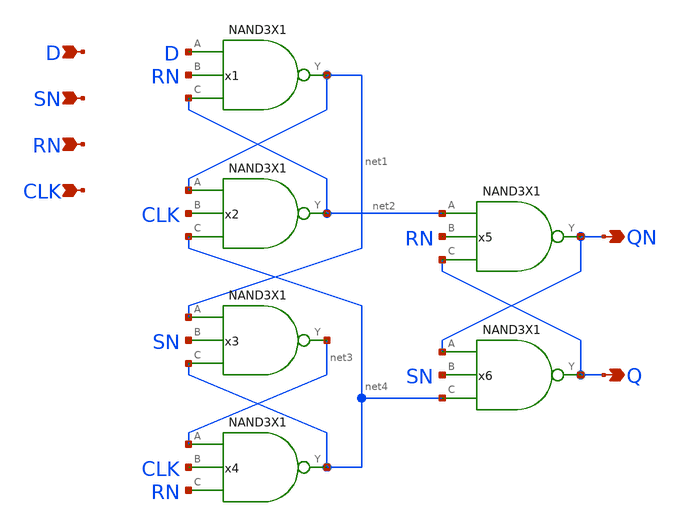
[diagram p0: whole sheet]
** sch_path: lib/xschem/DFFSNRNX1.sch
**.subckt DFFSNRNX1 D QN SN CLK Q RN
*.ipin D
*.opin QN
*.ipin SN
*.ipin CLK
*.opin Q
*.ipin RN
x3 net3 net1 SN net4 NAND3X1
x2 net2 net1 CLK net4 NAND3X1
x6 Q QN SN net4 NAND3X1
x1 net1 D RN net2 NAND3X1
x4 net4 net3 CLK RN NAND3X1
x5 QN net2 RN Q NAND3X1
**.ends

* expanding   symbol:  NAND3X1.sym # of pins=4
** sym_path: lib/xschem/NAND3X1.sym
** sch_path: lib/xschem/NAND3X1.sch
.subckt NAND3X1 Y A B C
*.ipin A
*.opin Y
*.ipin B
*.ipin C
XM1 net2 C GND GND sky130_fd_pr__nfet_01v8 L=0.15 W=3 nf=1 ad='int((nf+1)/2) * W/nf * 0.29' as='int((nf+2)/2) * W/nf * 0.29'
+ pd='2*int((nf+1)/2) * (W/nf + 0.29)' ps='2*int((nf+2)/2) * (W/nf + 0.29)' nrd='0.29 / W' nrs='0.29 / W'
+ sa=0 sb=0 sd=0 mult=1 m=1
XM2 Y A VDD VDD sky130_fd_pr__pfet_01v8 L=0.15 W=2 nf=1 ad='int((nf+1)/2) * W/nf * 0.29' as='int((nf+2)/2) * W/nf * 0.29'
+ pd='2*int((nf+1)/2) * (W/nf + 0.29)' ps='2*int((nf+2)/2) * (W/nf + 0.29)' nrd='0.29 / W' nrs='0.29 / W'
+ sa=0 sb=0 sd=0 mult=1 m=1
XM3 net1 B net2 GND sky130_fd_pr__nfet_01v8 L=0.15 W=3 nf=1 ad='int((nf+1)/2) * W/nf * 0.29' as='int((nf+2)/2) * W/nf * 0.29'
+ pd='2*int((nf+1)/2) * (W/nf + 0.29)' ps='2*int((nf+2)/2) * (W/nf + 0.29)' nrd='0.29 / W' nrs='0.29 / W'
+ sa=0 sb=0 sd=0 mult=1 m=1
XM4 Y A net1 GND sky130_fd_pr__nfet_01v8 L=0.15 W=3 nf=1 ad='int((nf+1)/2) * W/nf * 0.29' as='int((nf+2)/2) * W/nf * 0.29'
+ pd='2*int((nf+1)/2) * (W/nf + 0.29)' ps='2*int((nf+2)/2) * (W/nf + 0.29)' nrd='0.29 / W' nrs='0.29 / W'
+ sa=0 sb=0 sd=0 mult=1 m=1
XM5 Y A VDD VDD sky130_fd_pr__pfet_01v8 L=0.15 W=2 nf=1 ad='int((nf+1)/2) * W/nf * 0.29' as='int((nf+2)/2) * W/nf * 0.29'
+ pd='2*int((nf+1)/2) * (W/nf + 0.29)' ps='2*int((nf+2)/2) * (W/nf + 0.29)' nrd='0.29 / W' nrs='0.29 / W'
+ sa=0 sb=0 sd=0 mult=1 m=1
XM6 Y B VDD VDD sky130_fd_pr__pfet_01v8 L=0.15 W=2 nf=1 ad='int((nf+1)/2) * W/nf * 0.29' as='int((nf+2)/2) * W/nf * 0.29'
+ pd='2*int((nf+1)/2) * (W/nf + 0.29)' ps='2*int((nf+2)/2) * (W/nf + 0.29)' nrd='0.29 / W' nrs='0.29 / W'
+ sa=0 sb=0 sd=0 mult=1 m=1
XM7 Y B VDD VDD sky130_fd_pr__pfet_01v8 L=0.15 W=2 nf=1 ad='int((nf+1)/2) * W/nf * 0.29' as='int((nf+2)/2) * W/nf * 0.29'
+ pd='2*int((nf+1)/2) * (W/nf + 0.29)' ps='2*int((nf+2)/2) * (W/nf + 0.29)' nrd='0.29 / W' nrs='0.29 / W'
+ sa=0 sb=0 sd=0 mult=1 m=1
XM8 Y C VDD VDD sky130_fd_pr__pfet_01v8 L=0.15 W=2 nf=1 ad='int((nf+1)/2) * W/nf * 0.29' as='int((nf+2)/2) * W/nf * 0.29'
+ pd='2*int((nf+1)/2) * (W/nf + 0.29)' ps='2*int((nf+2)/2) * (W/nf + 0.29)' nrd='0.29 / W' nrs='0.29 / W'
+ sa=0 sb=0 sd=0 mult=1 m=1
XM9 Y C VDD VDD sky130_fd_pr__pfet_01v8 L=0.15 W=2 nf=1 ad='int((nf+1)/2) * W/nf * 0.29' as='int((nf+2)/2) * W/nf * 0.29'
+ pd='2*int((nf+1)/2) * (W/nf + 0.29)' ps='2*int((nf+2)/2) * (W/nf + 0.29)' nrd='0.29 / W' nrs='0.29 / W'
+ sa=0 sb=0 sd=0 mult=1 m=1
.ends

.GLOBAL VDD
.GLOBAL GND
.end
